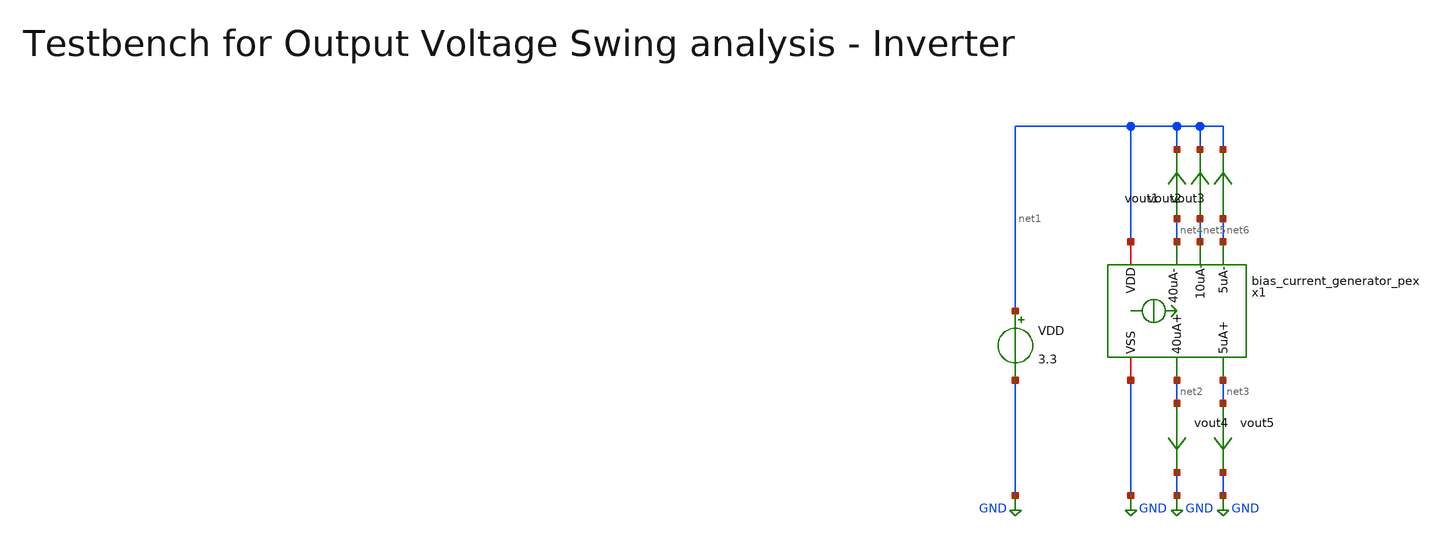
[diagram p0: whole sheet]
** sch_path: macros/heichips26_vcr/macros/switched_capacitor/testbenches/xschem/tb_bias_current_generator_pex_dc.sch
**.subckt tb_bias_current_generator_pex_dc
VDD net1 GND 3.3
vout1 net4 net1 0
.save i(vout1)
vout2 net5 net1 0
.save i(vout2)
vout3 net6 net1 0
.save i(vout3)
vout4 net2 GND 0
.save i(vout4)
vout5 net3 GND 0
.save i(vout5)
x1 net2 net3 net1 GND net6 net5 net4 bias_current_generator_pex
**** begin user architecture code


.include ../../../netlist/pex/bias_current_generator_magic_pex_3.spice
.param temp=27
.options savecurrents klu method=gear reltol=1e-3 abstol=1e-15 gmin=1e-15
.control

save all

* Operating Point Analysis
op
remzerovec
write @schname\.raw
set appendwrite

* DC Sweep
dc VDD 2.5 4 0.01
remzerovec
write @schname\.raw
set appendwrite

meas dc ymax MAX i(vout1)

* Plotting
plot i(vout1) i(vout2) i(vout3) i(vout4) i(vout5)
*plot i(vout1) ylimit 0 $&ymax
*plot deriv(i(vout1))/$&ymax*100 ylimit 0 4

dc temp -40 85 10

meas dc ymax MAX i(vout1)

* Plotting
*plot i(vout1) ylimit 0 $&ymax
*plot deriv(i(vout1))/$&ymax*100 ylimit -0.1 0.1

* Measurement
*meas dc Vgsp_at_Vcm when vout=Vcm
*print Vgsp_at_Vcm

* Write Data
*unset appendwrite
*set wr_vecnames
*set wr_singlescale
*wrdata ../plot_simulations/data/@schname\.txt v(vin) v(vout)

*quit
.endc



.lib cornerMOSlv.lib mos_tt
.lib cornerMOShv.lib mos_tt
.lib cornerRES.lib res_typ
.lib cornerDIO.lib dio_tt

**** end user architecture code
**.ends
.GLOBAL GND
.end
